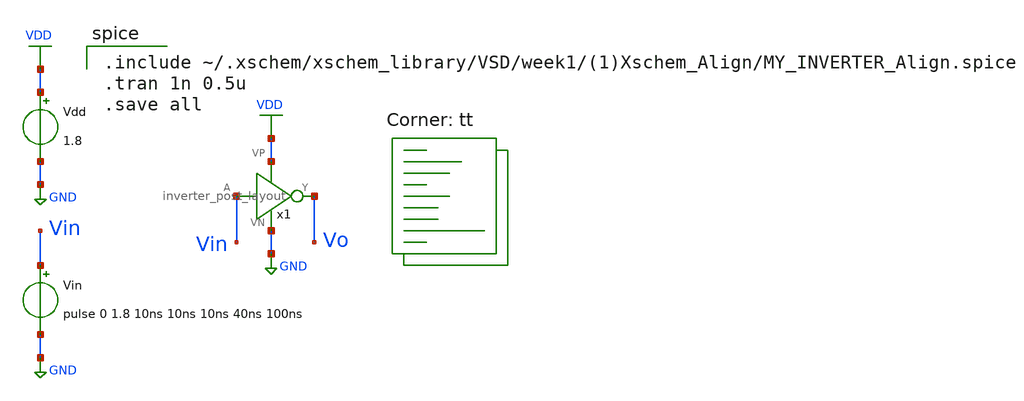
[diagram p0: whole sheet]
** sch_path: week 1/sim/2/inverter_tran_test_post_layout.sch
**.subckt inverter_tran_test_post_layout
Vdd VDD GND 1.8
Vin Vin GND pulse 0 1.8 10ns 10ns 10ns 40ns 100ns
x1 Vin VDD Vo GND inverter_post_layout
**** begin user architecture code

.include ~/.xschem/xschem_library/VSD/week1/(1)Xschem_Align/MY_INVERTER_Align.spice
.tran 1n 0.5u
.save all

 .lib /usr/local/share/pdk/sky130A/libs.tech/ngspice/sky130.lib.spice tt
**** end user architecture code
**.ends
.GLOBAL VDD
.GLOBAL GND
.end
